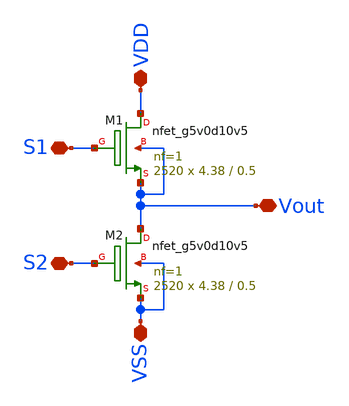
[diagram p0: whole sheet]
** sch_path: xschem/power_stage_3.sch
**.subckt power_stage_3 S1 Vout VDD VSS S2
*.iopin S1
*.iopin Vout
*.iopin VDD
*.iopin VSS
*.iopin S2
XM1 VDD S1 Vout Vout sky130_fd_pr__nfet_g5v0d10v5 L=0.5 W=4.38 nf=1 ad='int((nf+1)/2) * W/nf * 0.29'
+ as='int((nf+2)/2) * W/nf * 0.29' pd='2*int((nf+1)/2) * (W/nf + 0.29)' ps='2*int((nf+2)/2) * (W/nf + 0.29)'
+ nrd='0.29 / W' nrs='0.29 / W' sa=0 sb=0 sd=0 mult=2520 m=2520
XM2 Vout S2 VSS VSS sky130_fd_pr__nfet_g5v0d10v5 L=0.5 W=4.38 nf=1 ad='int((nf+1)/2) * W/nf * 0.29' as='int((nf+2)/2) * W/nf * 0.29'
+ pd='2*int((nf+1)/2) * (W/nf + 0.29)' ps='2*int((nf+2)/2) * (W/nf + 0.29)' nrd='0.29 / W' nrs='0.29 / W'
+ sa=0 sb=0 sd=0 mult=2520 m=2520
**.ends
.end
